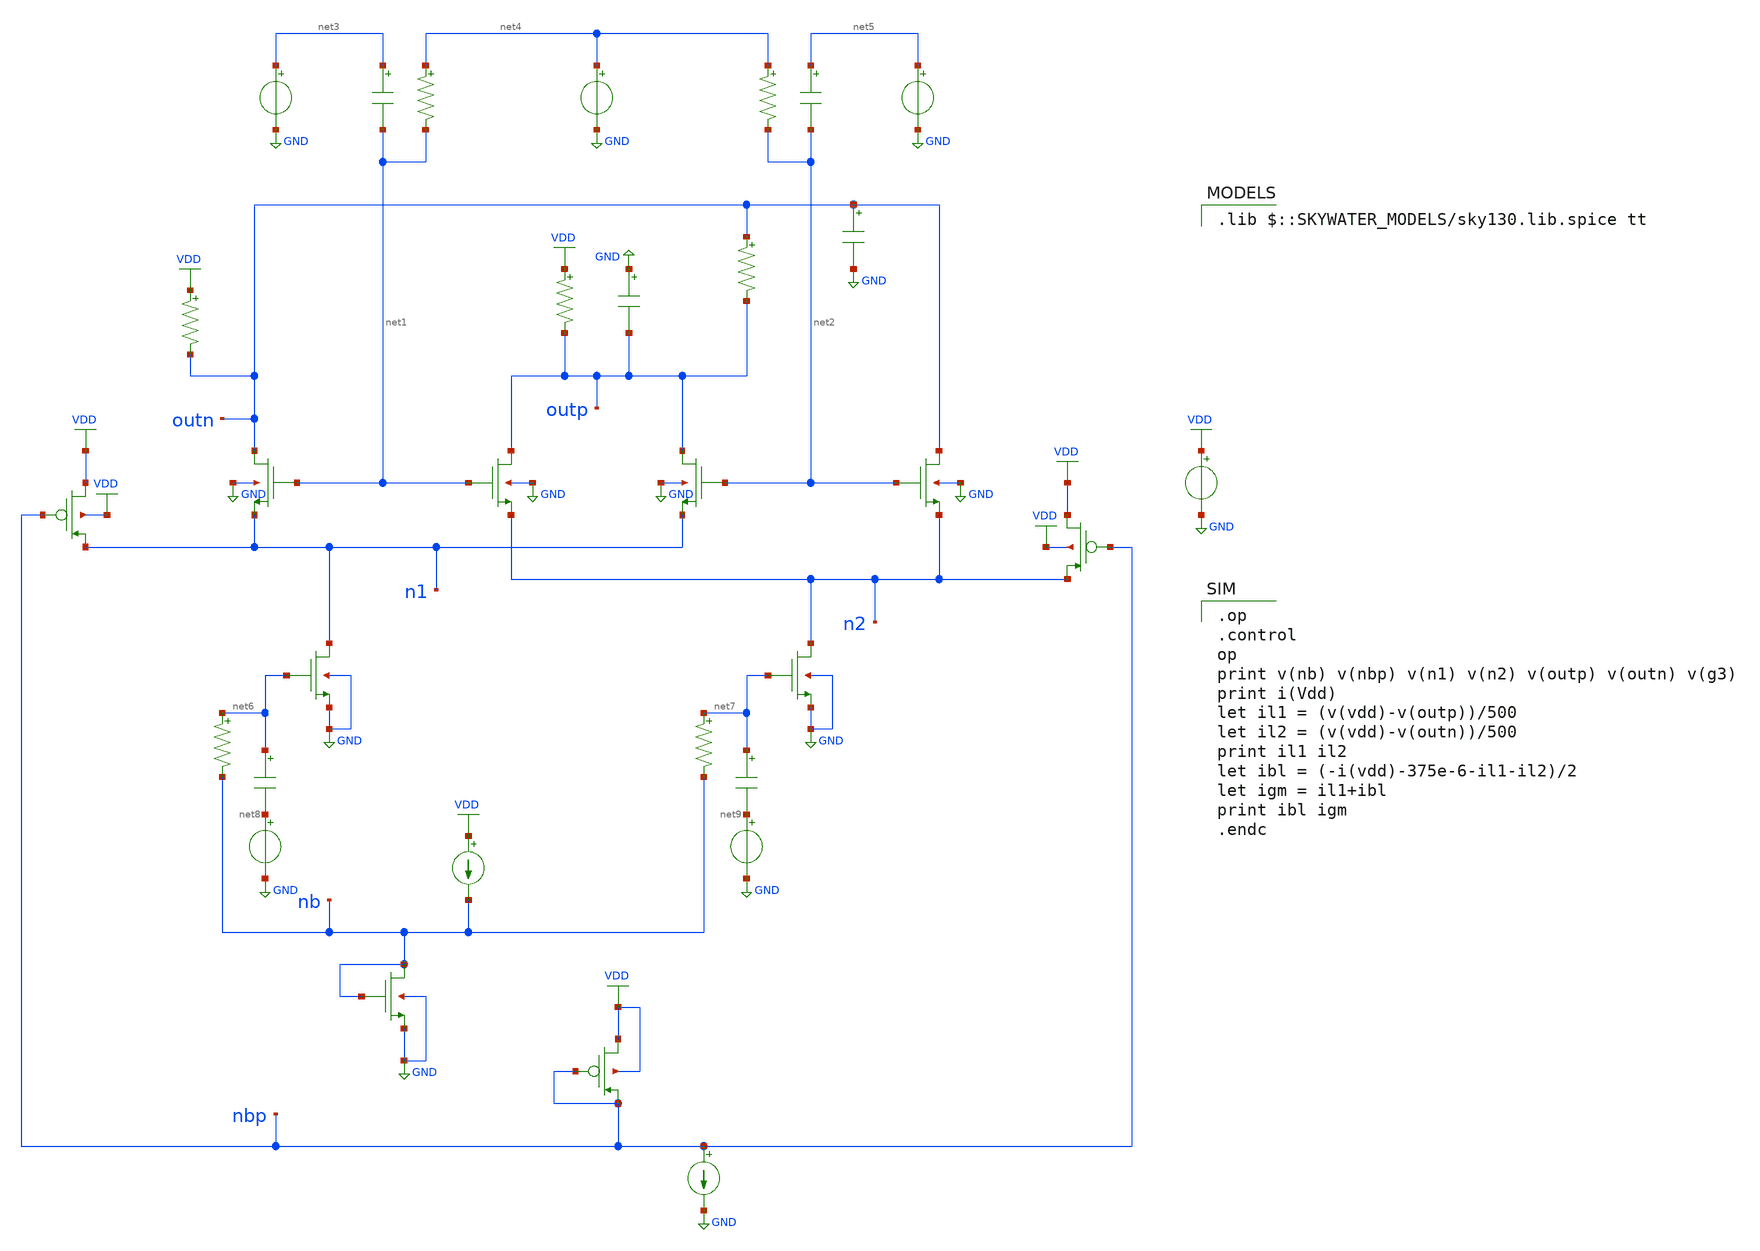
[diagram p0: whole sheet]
** sch_path: 09-sky130-gilbert-mixer-rfic/schematics/3_gilbert_mixer.sch
**.subckt 3_gilbert_mixer
XM3 outn net1 n1 GND sky130_fd_pr__nfet_01v8 L=0.15 W=10 nf=1 ad='int((nf+1)/2) * W/nf * 0.29' as='int((nf+2)/2) * W/nf * 0.29'
+ pd='2*int((nf+1)/2) * (W/nf + 0.29)' ps='2*int((nf+2)/2) * (W/nf + 0.29)' nrd='0.29 / W' nrs='0.29 / W'
+ sa=0 sb=0 sd=0 mult=1 m=1
XM5 outp net1 n2 GND sky130_fd_pr__nfet_01v8 L=0.15 W=10 nf=1 ad='int((nf+1)/2) * W/nf * 0.29' as='int((nf+2)/2) * W/nf * 0.29'
+ pd='2*int((nf+1)/2) * (W/nf + 0.29)' ps='2*int((nf+2)/2) * (W/nf + 0.29)' nrd='0.29 / W' nrs='0.29 / W'
+ sa=0 sb=0 sd=0 mult=1 m=1
XM4 outp net2 n1 GND sky130_fd_pr__nfet_01v8 L=0.15 W=10 nf=1 ad='int((nf+1)/2) * W/nf * 0.29' as='int((nf+2)/2) * W/nf * 0.29'
+ pd='2*int((nf+1)/2) * (W/nf + 0.29)' ps='2*int((nf+2)/2) * (W/nf + 0.29)' nrd='0.29 / W' nrs='0.29 / W'
+ sa=0 sb=0 sd=0 mult=1 m=1
XM6 outn net2 n2 GND sky130_fd_pr__nfet_01v8 L=0.15 W=10 nf=1 ad='int((nf+1)/2) * W/nf * 0.29' as='int((nf+2)/2) * W/nf * 0.29'
+ pd='2*int((nf+1)/2) * (W/nf + 0.29)' ps='2*int((nf+2)/2) * (W/nf + 0.29)' nrd='0.29 / W' nrs='0.29 / W'
+ sa=0 sb=0 sd=0 mult=1 m=1
Clop net3 net1 4p m=1
Rlop net4 net1 5k m=1
Clon net5 net2 4p m=1
Rlon net4 net2 5k m=1
Vlop net3 GND 0
Vlocm net4 GND 1.4
Vlon net5 GND 0
Rload2 VDD outn 500 m=1
Rload1 VDD outp 500 m=1
Cl1 GND outp 2p m=1
Rext outn outp 20k m=1
Cl2 outn GND 2p m=1
XMP1 VDD nbp n1 VDD sky130_fd_pr__pfet_01v8 L=0.5 W=4 nf=1 ad='int((nf+1)/2) * W/nf * 0.29' as='int((nf+2)/2) * W/nf * 0.29'
+ pd='2*int((nf+1)/2) * (W/nf + 0.29)' ps='2*int((nf+2)/2) * (W/nf + 0.29)' nrd='0.29 / W' nrs='0.29 / W'
+ sa=0 sb=0 sd=0 mult=8 m=8
XMP2 VDD nbp n2 VDD sky130_fd_pr__pfet_01v8 L=0.5 W=4 nf=1 ad='int((nf+1)/2) * W/nf * 0.29' as='int((nf+2)/2) * W/nf * 0.29'
+ pd='2*int((nf+1)/2) * (W/nf + 0.29)' ps='2*int((nf+2)/2) * (W/nf + 0.29)' nrd='0.29 / W' nrs='0.29 / W'
+ sa=0 sb=0 sd=0 mult=8 m=8
XM1 n1 net6 GND GND sky130_fd_pr__nfet_01v8 L=0.15 W=4 nf=1 ad='int((nf+1)/2) * W/nf * 0.29' as='int((nf+2)/2) * W/nf * 0.29'
+ pd='2*int((nf+1)/2) * (W/nf + 0.29)' ps='2*int((nf+2)/2) * (W/nf + 0.29)' nrd='0.29 / W' nrs='0.29 / W'
+ sa=0 sb=0 sd=0 mult=20 m=20
Rbg1 net6 nb 10k m=1
Cc1 net6 net8 2p m=1
Vrfp net8 GND 0
XM2 n2 net7 GND GND sky130_fd_pr__nfet_01v8 L=0.15 W=4 nf=1 ad='int((nf+1)/2) * W/nf * 0.29' as='int((nf+2)/2) * W/nf * 0.29'
+ pd='2*int((nf+1)/2) * (W/nf + 0.29)' ps='2*int((nf+2)/2) * (W/nf + 0.29)' nrd='0.29 / W' nrs='0.29 / W'
+ sa=0 sb=0 sd=0 mult=20 m=20
Rbg2 net7 nb 10k m=1
Cc2 net7 net9 2p m=1
Vrfn net9 GND 0
Iref VDD nb 250u
XMb nb nb GND GND sky130_fd_pr__nfet_01v8 L=0.15 W=4 nf=1 ad='int((nf+1)/2) * W/nf * 0.29' as='int((nf+2)/2) * W/nf * 0.29'
+ pd='2*int((nf+1)/2) * (W/nf + 0.29)' ps='2*int((nf+2)/2) * (W/nf + 0.29)' nrd='0.29 / W' nrs='0.29 / W'
+ sa=0 sb=0 sd=0 mult=2 m=2
XMPb VDD nbp nbp VDD sky130_fd_pr__pfet_01v8 L=0.5 W=4 nf=1 ad='int((nf+1)/2) * W/nf * 0.29' as='int((nf+2)/2) * W/nf * 0.29'
+ pd='2*int((nf+1)/2) * (W/nf + 0.29)' ps='2*int((nf+2)/2) * (W/nf + 0.29)' nrd='0.29 / W' nrs='0.29 / W'
+ sa=0 sb=0 sd=0 mult=1 m=1
Ibp nbp GND 125u
Vdd VDD GND 1.8
**** begin user architecture code
 .lib $::SKYWATER_MODELS/sky130.lib.spice tt

.op
.control
op
print v(nb) v(nbp) v(n1) v(n2) v(outp) v(outn) v(g3)
print i(Vdd)
let il1 = (v(vdd)-v(outp))/500
let il2 = (v(vdd)-v(outn))/500
print il1 il2
let ibl = (-i(vdd)-375e-6-il1-il2)/2
let igm = il1+ibl
print ibl igm
.endc

**** end user architecture code
**.ends
.GLOBAL GND
.GLOBAL VDD
.end
